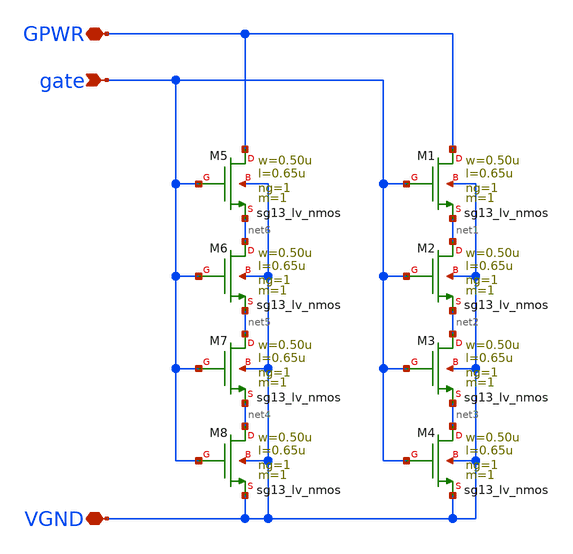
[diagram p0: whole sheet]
** sch_path: ihp-sg13cmos5l/libs.tech/xschem/hm_analog/dischg.sch
**.subckt dischg GPWR VGND gate
*.iopin GPWR
*.iopin VGND
*.ipin gate
XM1 GPWR gate net1 VGND sg13_lv_nmos w=0.50u l=0.65u ng=1 m=1 mm_ok=1
XM2 net1 gate net2 VGND sg13_lv_nmos w=0.50u l=0.65u ng=1 m=1 mm_ok=1
XM3 net2 gate net3 VGND sg13_lv_nmos w=0.50u l=0.65u ng=1 m=1 mm_ok=1
XM4 net3 gate VGND VGND sg13_lv_nmos w=0.50u l=0.65u ng=1 m=1 mm_ok=1
XM5 GPWR gate net6 VGND sg13_lv_nmos w=0.50u l=0.65u ng=1 m=1 mm_ok=1
XM6 net6 gate net5 VGND sg13_lv_nmos w=0.50u l=0.65u ng=1 m=1 mm_ok=1
XM7 net5 gate net4 VGND sg13_lv_nmos w=0.50u l=0.65u ng=1 m=1 mm_ok=1
XM8 net4 gate VGND VGND sg13_lv_nmos w=0.50u l=0.65u ng=1 m=1 mm_ok=1
**.ends
.end
